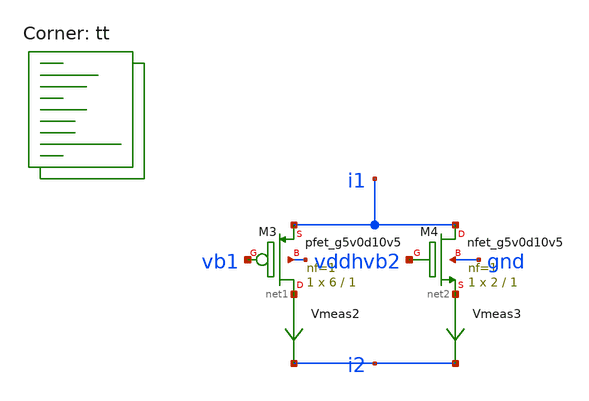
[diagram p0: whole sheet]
** sch_path: xschem/op_amp_monticelli_biasing.sch
**.subckt op_amp_monticelli_biasing
XM3 net1 vb1 i1 vddh sky130_fd_pr__pfet_g5v0d10v5 L=1 W=6 nf=1 ad='int((nf+1)/2) * W/nf * 0.29' as='int((nf+2)/2) * W/nf * 0.29'
+ pd='2*int((nf+1)/2) * (W/nf + 0.29)' ps='2*int((nf+2)/2) * (W/nf + 0.29)' nrd='0.29 / W' nrs='0.29 / W'
+ sa=0 sb=0 sd=0 mult=1 m=1
XM4 i1 vb2 net2 gnd sky130_fd_pr__nfet_g5v0d10v5 L=1 W=2 nf=1 ad='int((nf+1)/2) * W/nf * 0.29' as='int((nf+2)/2) * W/nf * 0.29'
+ pd='2*int((nf+1)/2) * (W/nf + 0.29)' ps='2*int((nf+2)/2) * (W/nf + 0.29)' nrd='0.29 / W' nrs='0.29 / W'
+ sa=0 sb=0 sd=0 mult=1 m=1
Vmeas2 net1 i2 0
.save i(vmeas2)
Vmeas3 net2 i2 0
.save i(vmeas3)
**** begin user architecture code
.lib $::SKYWATER_MODELS/sky130.lib.spice tt



  .option wnflag=1
  .option safecurrents
  ********************Static Current Sources***************************
  .param iref=1u
  I1 vddh i1 iref
  I2 i2 gnd 1u
  ********************Static Voltage Sources***************************
  Vddh vddh gnd dc 5.5

  vb1 vb1 gnd dc 2.7749
  vb2 vb2 gnd dc 2.2
  ********************Dynamic Voltage Sources***************************
  *******Calculation**********
  .param base_f=100e3 base_t={1/base_f} base_th={base_t/2} base_d={base_th}
  .param d2_th ={base_th} d2_t={2*d2_th}
  .param d1_th ={4*d2_th} d1_t={d0_th}
  .param d0_th ={4*d1_th} d0_t={4*d0_th}

  .param d20_d ={0} d21_d={1*d2_th} d22_d={2*d2_th} d23_d={3*d2_th}
  .param d10_d ={0} d11_d={1*d1_th} d12_d={2*d1_th} d13_d={3*d1_th}
  .param d00_d ={0} d01_d={1*d0_th} d02_d={2*d0_th} d03_d={3*d0_th}
  *******Signals**********
  .param vhi=5.5
*  Vin1 b[0] gnd pulse(0 {vhi} {0} 1p 1p {10u} {20u})
*  Vin2 b[1] gnd pulse(0 {vhi} {0} 1p 1p {20u} {40u})
  ********************Simulation Commands*****************************
  .control
     reset
     save all
*     tran 0.1n 100n
    dc vb1 2 4 0.01
     write monticelli-tb.raw
     set appendwrite
*    quit 0
  .endc



**** end user architecture code
**.ends
.end
